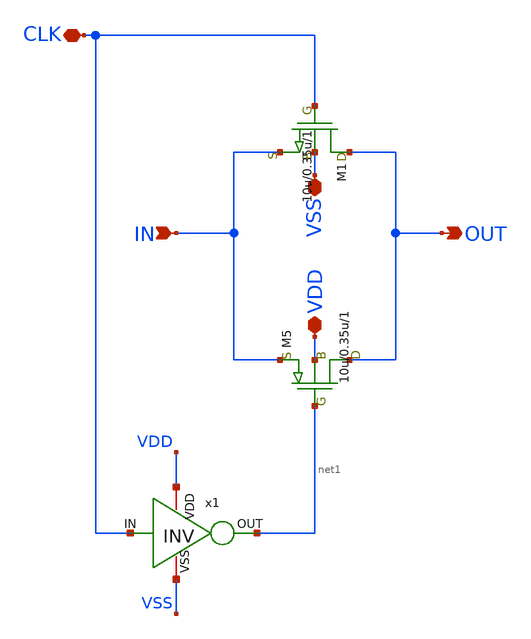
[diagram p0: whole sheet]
** sch_path: CMOSSW.sch
**.subckt CMOSSW IN VSS OUT CLK VDD
*.ipin IN
*.iopin VSS
*.opin OUT
*.iopin CLK
*.iopin VDD
M1 OUT CLK IN VSS nch w=10u l=0.35u as=0 ps=0 ad=0 pd=0 m=1
M5 OUT net1 IN VDD pch w=10u l=0.35u as=0 ps=0 ad=0 pd=0 m=1
x1 VDD net1 CLK VSS INV
**.ends

* expanding   symbol:  INV.sym # of pins=4
** sym_path: INV.sym
** sch_path: INV.sch
.subckt INV VDD OUT IN VSS
*.opin OUT
*.ipin IN
*.iopin VDD
*.iopin VSS
M2 OUT IN VDD VDD pch w=10u l=0.35u as=0 ps=0 ad=0 pd=0 m=1
M1 OUT IN VSS VSS nch w=5u l=0.35u as=0 ps=0 ad=0 pd=0 m=1
.ends

.end
